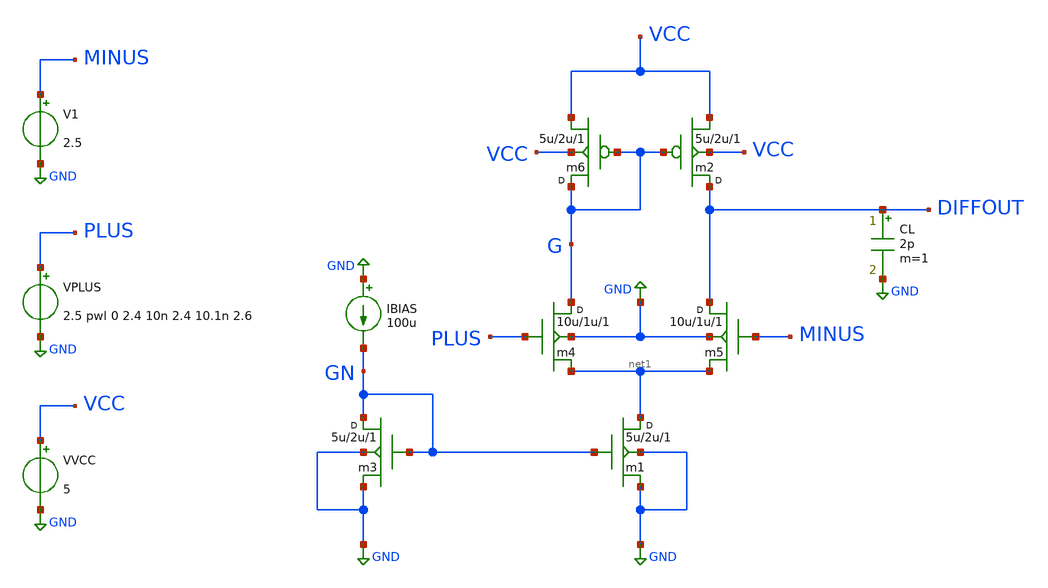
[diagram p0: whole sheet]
** sch_path: diff_amp.sch
**.subckt diff_amp
m2 DIFFOUT G VCC VCC pmos w=5u l=2u m=1
m4 G PLUS net1 GND nmos w=10u l=1u m=1
m6 G G VCC VCC pmos w=5u l=2u m=1
m5 DIFFOUT MINUS net1 GND nmos w=10u l=1u m=1
m1 net1 GN GND GND nmos w=5u l=2u m=1
m3 GN GN GND GND nmos w=5u l=2u m=1
CL DIFFOUT GND 2p m=1
IBIAS GND GN 100u
V1 MINUS GND 2.5
VPLUS PLUS GND 2.5 pwl 0 2.4 10n 2.4 10.1n 2.6
VVCC VCC GND 5
**** begin user architecture code


.temp 30
.tran 10n 2000u uic
.save all


**** end user architecture code
**.ends
.GLOBAL GND
.end
